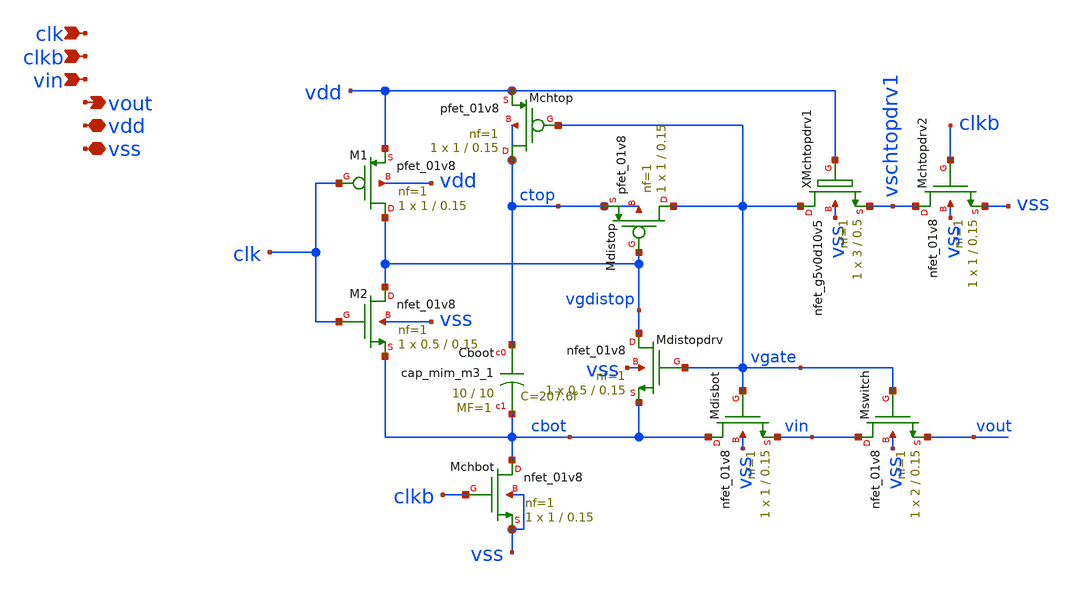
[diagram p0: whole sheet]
** sch_path: xschem/sar-adc/bootstrap.sch
**.subckt bootstrap clk clkb vin vout vdd vss
*.ipin clk
*.ipin clkb
*.ipin vin
*.opin vout
*.iopin vdd
*.iopin vss
XMswitch vin vgate vout vss sky130_fd_pr__nfet_01v8 L=0.15 W=2 nf=1 ad='int((1 + 1)/2) * 2 / 1 * 0.29'
+ as='int((1 + 2)/2) * 2 / 1 * 0.29' pd='2*int((1 + 1)/2) * (2 / 1 + 0.29)' ps='2*int((1 + 2)/2) * (2 / 1 + 0.29)'
+ nrd='0.29 / 2 ' nrs='0.29 / 2 ' sa=0 sb=0 sd=0 mult=1 m=1
XMdisbot cbot vgate vin vss sky130_fd_pr__nfet_01v8 L=0.15 W=1 nf=1 ad='int((1 + 1)/2) * 1 / 1 * 0.29'
+ as='int((1 + 2)/2) * 1 / 1 * 0.29' pd='2*int((1 + 1)/2) * (1 / 1 + 0.29)' ps='2*int((1 + 2)/2) * (1 / 1 + 0.29)'
+ nrd='0.29 / 1 ' nrs='0.29 / 1 ' sa=0 sb=0 sd=0 mult=1 m=1
XCboot ctop cbot sky130_fd_pr__cap_mim_m3_1 W=10 L=10 MF=1 m=1
XMdistop vgate vgdistop ctop ctop sky130_fd_pr__pfet_01v8 L=0.15 W=1 nf=1 ad='int((1 + 1)/2) * 1 / 1 * 0.29'
+ as='int((1 + 2)/2) * 1 / 1 * 0.29' pd='2*int((1 + 1)/2) * (1 / 1 + 0.29)' ps='2*int((1 + 2)/2) * (1 / 1 + 0.29)'
+ nrd='0.29 / 1 ' nrs='0.29 / 1 ' sa=0 sb=0 sd=0 mult=1 m=1
XMchtop ctop vgate vdd ctop sky130_fd_pr__pfet_01v8 L=0.15 W=1 nf=1 ad='int((1 + 1)/2) * 1 / 1 * 0.29'
+ as='int((1 + 2)/2) * 1 / 1 * 0.29' pd='2*int((1 + 1)/2) * (1 / 1 + 0.29)' ps='2*int((1 + 2)/2) * (1 / 1 + 0.29)'
+ nrd='0.29 / 1 ' nrs='0.29 / 1 ' sa=0 sb=0 sd=0 mult=1 m=1
XMdistopdrv vgdistop vgate cbot vss sky130_fd_pr__nfet_01v8 L=0.15 W=0.5 nf=1 ad='int((1 + 1)/2) * 0.5 / 1 * 0.29'
+ as='int((1 + 2)/2) * 0.5 / 1 * 0.29' pd='2*int((1 + 1)/2) * (0.5 / 1 + 0.29)' ps='2*int((1 + 2)/2) * (0.5 / 1 + 0.29)'
+ nrd='0.29 / 0.5 ' nrs='0.29 / 0.5 ' sa=0 sb=0 sd=0 mult=1 m=1
XMchtopdrv2 vschtopdrv1 clkb vss vss sky130_fd_pr__nfet_01v8 L=0.15 W=1 nf=1 ad='int((1 + 1)/2) * 1 / 1 * 0.29'
+ as='int((1 + 2)/2) * 1 / 1 * 0.29' pd='2*int((1 + 1)/2) * (1 / 1 + 0.29)' ps='2*int((1 + 2)/2) * (1 / 1 + 0.29)'
+ nrd='0.29 / 1 ' nrs='0.29 / 1 ' sa=0 sb=0 sd=0 mult=1 m=1
XMchbot cbot clkb vss vss sky130_fd_pr__nfet_01v8 L=0.15 W=1 nf=1 ad='int((1 + 1)/2) * 1 / 1 * 0.29'
+ as='int((1 + 2)/2) * 1 / 1 * 0.29' pd='2*int((1 + 1)/2) * (1 / 1 + 0.29)' ps='2*int((1 + 2)/2) * (1 / 1 + 0.29)'
+ nrd='0.29 / 1 ' nrs='0.29 / 1 ' sa=0 sb=0 sd=0 mult=1 m=1
XM1 vgdistop clk vdd vdd sky130_fd_pr__pfet_01v8 L=0.15 W=1 nf=1 ad='int((1 + 1)/2) * 1 / 1 * 0.29' as='int((1 + 2)/2) * 1 / 1 * 0.29'
+ pd='2*int((1 + 1)/2) * (1 / 1 + 0.29)' ps='2*int((1 + 2)/2) * (1 / 1 + 0.29)' nrd='0.29 / 1 ' nrs='0.29 / 1 '
+ sa=0 sb=0 sd=0 mult=1 m=1
XM2 vgdistop clk cbot vss sky130_fd_pr__nfet_01v8 L=0.15 W=0.5 nf=1 ad='int((1 + 1)/2) * 0.5 / 1 * 0.29'
+ as='int((1 + 2)/2) * 0.5 / 1 * 0.29' pd='2*int((1 + 1)/2) * (0.5 / 1 + 0.29)' ps='2*int((1 + 2)/2) * (0.5 / 1 + 0.29)'
+ nrd='0.29 / 0.5 ' nrs='0.29 / 0.5 ' sa=0 sb=0 sd=0 mult=1 m=1
XXMchtopdrv1 vgate vdd vschtopdrv1 vss sky130_fd_pr__nfet_g5v0d10v5 L=0.5 W=3 nf=1 ad='int((1 + 1)/2) * 3 / 1 * 0.29'
+ as='int((1 + 2)/2) * 3 / 1 * 0.29' pd='2*int((1 + 1)/2) * (3 / 1 + 0.29)' ps='2*int((1 + 2)/2) * (3 / 1 + 0.29)'
+ nrd='0.29 / 3 ' nrs='0.29 / 3 ' sa=0 sb=0 sd=0 mult=1 m=1
**.ends
.end
